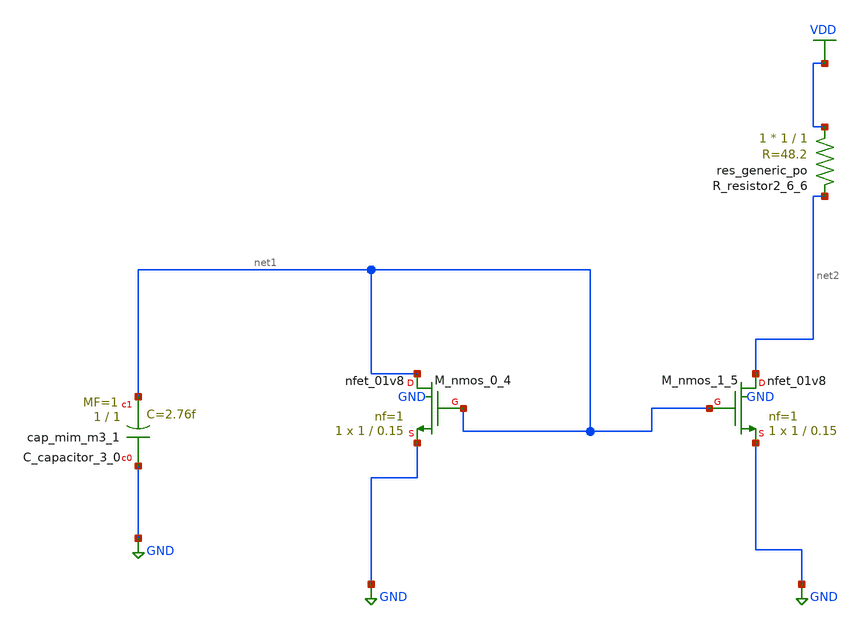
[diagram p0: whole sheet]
** sch_path: schematics/AMSNet/339.sch
**.subckt 339
XC_capacitor_3_0 GND net1 sky130_fd_pr__cap_mim_m3_1 W=1 L=1 MF=1 m=1
XM_nmos_0_4 net1 net1 GND GND sky130_fd_pr__nfet_01v8 L=0.15 W=1 nf=1 ad='int((1 + 1)/2) * 1 / 1 * 0.29'
+ as='int((1 + 2)/2) * 1 / 1 * 0.29' pd='2*int((1 + 1)/2) * (1 / 1 + 0.29)' ps='2*int((1 + 2)/2) * (1 / 1 + 0.29)'
+ nrd='0.29 / 1 ' nrs='0.29 / 1 ' sa=0 sb=0 sd=0 mult=1 m=1
XM_nmos_1_5 net2 net1 GND GND sky130_fd_pr__nfet_01v8 L=0.15 W=1 nf=1 ad='int((1 + 1)/2) * 1 / 1 * 0.29'
+ as='int((1 + 2)/2) * 1 / 1 * 0.29' pd='2*int((1 + 1)/2) * (1 / 1 + 0.29)' ps='2*int((1 + 2)/2) * (1 / 1 + 0.29)'
+ nrd='0.29 / 1 ' nrs='0.29 / 1 ' sa=0 sb=0 sd=0 mult=1 m=1
XR_resistor2_6_6 VDD net2 sky130_fd_pr__res_generic_po W=1 L=1 m=1
**.ends
.GLOBAL GND
.GLOBAL VDD
.end
